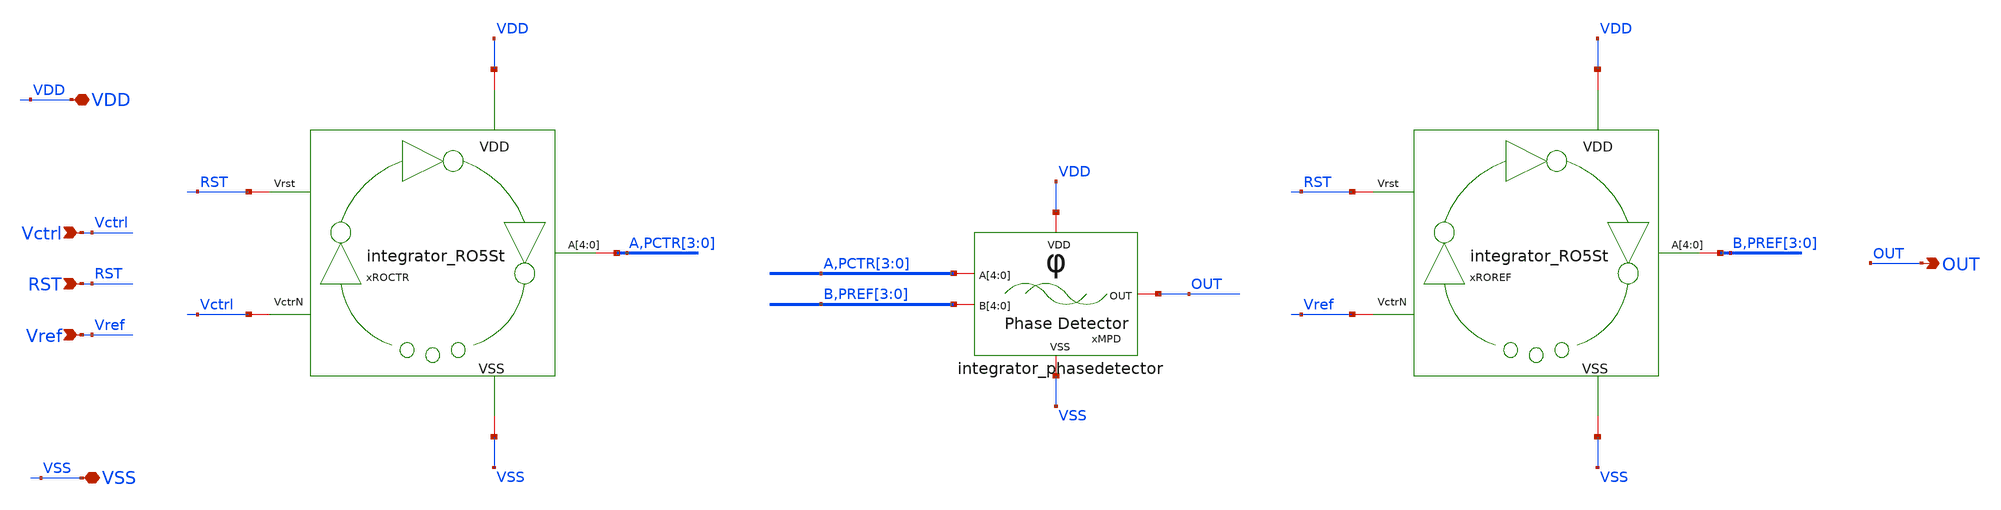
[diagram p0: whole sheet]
** sch_path: designs/ring_oscillator_pg/integrator/xschem/integrator.sch
**.subckt integrator Vctrl RST Vref VDD VSS OUT
*.ipin Vctrl
*.ipin RST
*.ipin Vref
*.iopin VDD
*.iopin VSS
*.opin OUT
xROCTR VDD VSS Vctrl RST A PCTR[3] PCTR[2] PCTR[1] PCTR[0] integrator_RO5St
xROREF VDD VSS Vref RST B PREF[3] PREF[2] PREF[1] PREF[0] integrator_RO5St
xMPD VDD VSS A PCTR[3] PCTR[2] PCTR[1] PCTR[0] B PREF[3] PREF[2] PREF[1] PREF[0] OUT
+ integrator_phasedetector
**.ends
.end
